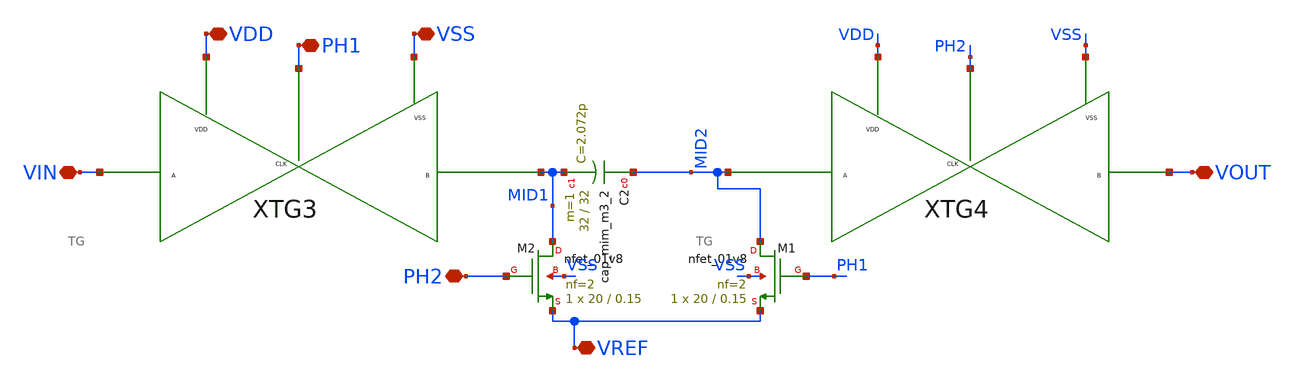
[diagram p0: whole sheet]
** sch_path: xschem/xschem_BGR_Top/Sigma_Delta/SC_Resistor/SC_Resistor.sch
**.subckt SC_Resistor VDD PH1 VIN VOUT PH2 VREF VSS
*.iopin VDD
*.iopin PH1
*.iopin VIN
*.iopin VOUT
*.iopin PH2
*.iopin VREF
*.iopin VSS
XTG3 VSS PH1 VDD VIN MID1 TG
XTG4 VSS PH2 VDD MID2 VOUT TG
XM2 MID1 PH2 VREF VSS sky130_fd_pr__nfet_01v8 L=0.15 W=20 nf=2 ad='int((nf+1)/2) * W/nf * 0.29' as='int((nf+2)/2) * W/nf * 0.29'
+ pd='2*int((nf+1)/2) * (W/nf + 0.29)' ps='2*int((nf+2)/2) * (W/nf + 0.29)' nrd='0.29 / W' nrs='0.29 / W'
+ sa=0 sb=0 sd=0 mult=1 m=1
XM1 MID2 PH1 VREF VSS sky130_fd_pr__nfet_01v8 L=0.15 W=20 nf=2 ad='int((nf+1)/2) * W/nf * 0.29' as='int((nf+2)/2) * W/nf * 0.29'
+ pd='2*int((nf+1)/2) * (W/nf + 0.29)' ps='2*int((nf+2)/2) * (W/nf + 0.29)' nrd='0.29 / W' nrs='0.29 / W'
+ sa=0 sb=0 sd=0 mult=1 m=1
XC2 MID2 MID1 sky130_fd_pr__cap_mim_m3_2 W=32 L=32 MF=1 m=1
**** begin user architecture code

** opencircuitdesign pdks install
.lib $::SKYWATER_MODELS/sky130.lib.spice tt


**** end user architecture code
**.ends

* expanding   symbol:  Sigma_Delta/Transmission_Gate/TG.sym # of pins=5
** sym_path: xschem/xschem_BGR_Top/Sigma_Delta/Transmission_Gate/TG.sym
** sch_path: xschem/xschem_BGR_Top/Sigma_Delta/Transmission_Gate/TG.sch
.subckt TG VSS CLK VDD A B
*.iopin VDD
*.iopin VSS
*.iopin A
*.iopin B
*.iopin CLK
XM1 A CLK B VSS sky130_fd_pr__nfet_01v8 L=0.15 W=10 nf=1 ad='int((nf+1)/2) * W/nf * 0.29' as='int((nf+2)/2) * W/nf * 0.29'
+ pd='2*int((nf+1)/2) * (W/nf + 0.29)' ps='2*int((nf+2)/2) * (W/nf + 0.29)' nrd='0.29 / W' nrs='0.29 / W'
+ sa=0 sb=0 sd=0 mult=1 m=1
XM2 B CLKB A VDD sky130_fd_pr__pfet_01v8 L=0.15 W=20 nf=2 ad='int((nf+1)/2) * W/nf * 0.29' as='int((nf+2)/2) * W/nf * 0.29'
+ pd='2*int((nf+1)/2) * (W/nf + 0.29)' ps='2*int((nf+2)/2) * (W/nf + 0.29)' nrd='0.29 / W' nrs='0.29 / W'
+ sa=0 sb=0 sd=0 mult=1 m=1
XM3 CLKB CLK VSS VSS sky130_fd_pr__nfet_01v8 L=0.15 W=10 nf=5 ad='int((nf+1)/2) * W/nf * 0.29' as='int((nf+2)/2) * W/nf * 0.29'
+ pd='2*int((nf+1)/2) * (W/nf + 0.29)' ps='2*int((nf+2)/2) * (W/nf + 0.29)' nrd='0.29 / W' nrs='0.29 / W'
+ sa=0 sb=0 sd=0 mult=1 m=1
XM4 CLKB CLK VDD VDD sky130_fd_pr__pfet_01v8 L=0.15 W=20 nf=10 ad='int((nf+1)/2) * W/nf * 0.29' as='int((nf+2)/2) * W/nf * 0.29'
+ pd='2*int((nf+1)/2) * (W/nf + 0.29)' ps='2*int((nf+2)/2) * (W/nf + 0.29)' nrd='0.29 / W' nrs='0.29 / W'
+ sa=0 sb=0 sd=0 mult=1 m=1
.ends

.end
